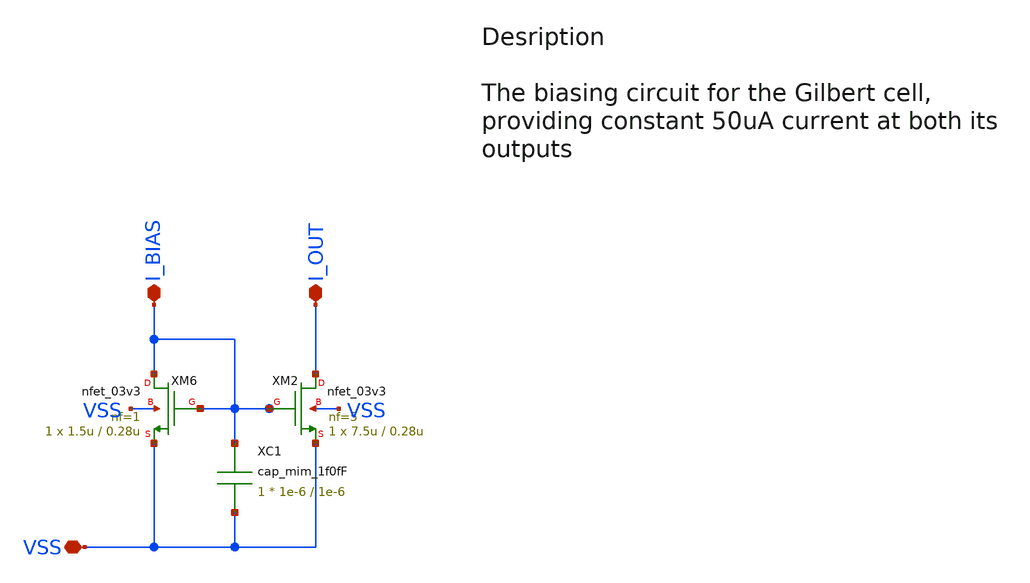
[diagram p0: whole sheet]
** sch_path: src/python/Cmirror_with_decap/xschem/nmos_Cmirror_with_decap.sch
**.subckt nmos_Cmirror_with_decap VSS I_OUT I_BIAS
*.iopin VSS
*.iopin I_OUT
*.iopin I_BIAS
XM2 I_OUT I_BIAS VSS VSS nfet_03v3 L=0.28u W=7.5u nf=5 ad='int((nf+1)/2) * W/nf * 0.18u' as='int((nf+2)/2) * W/nf * 0.18u'
+ pd='2*int((nf+1)/2) * (W/nf + 0.18u)' ps='2*int((nf+2)/2) * (W/nf + 0.18u)' nrd='0.18u / W' nrs='0.18u / W'
+ sa=0 sb=0 sd=0 m=1
XM6 I_BIAS I_BIAS VSS VSS nfet_03v3 L=0.28u W=1.5u nf=1 ad='int((nf+1)/2) * W/nf * 0.18u' as='int((nf+2)/2) * W/nf * 0.18u'
+ pd='2*int((nf+1)/2) * (W/nf + 0.18u)' ps='2*int((nf+2)/2) * (W/nf + 0.18u)' nrd='0.18u / W' nrs='0.18u / W'
+ sa=0 sb=0 sd=0 m=1
XC1 I_BIAS VSS cap_mim_1f0fF c_width=1e-6 c_length=1e-6 m=1
**** begin user architecture code

.include $::180MCU_MODELS/design.ngspice
.lib $::180MCU_MODELS/sm141064.ngspice typical
.lib $::180MCU_MODELS/sm141064.ngspice mimcap_typical
.lib $::180MCU_MODELS/sm141064.ngspice cap_mim
.lib $::180MCU_MODELS/sm141064.ngspice res_typical




* let sets vectors to a plot, while set sets a variable, globally accessible in .control
.control

    * Set frequency and amplitude variables to proper values from within the control sequence
    save all

    op
    show

    write Biasing_network_sim.raw

    set appendwrite

    * Transient analysis to observe mixing operation
    tran 1p 10n


    write Biasing_network_sim.raw

.endc


**** end user architecture code
**.ends
.end
